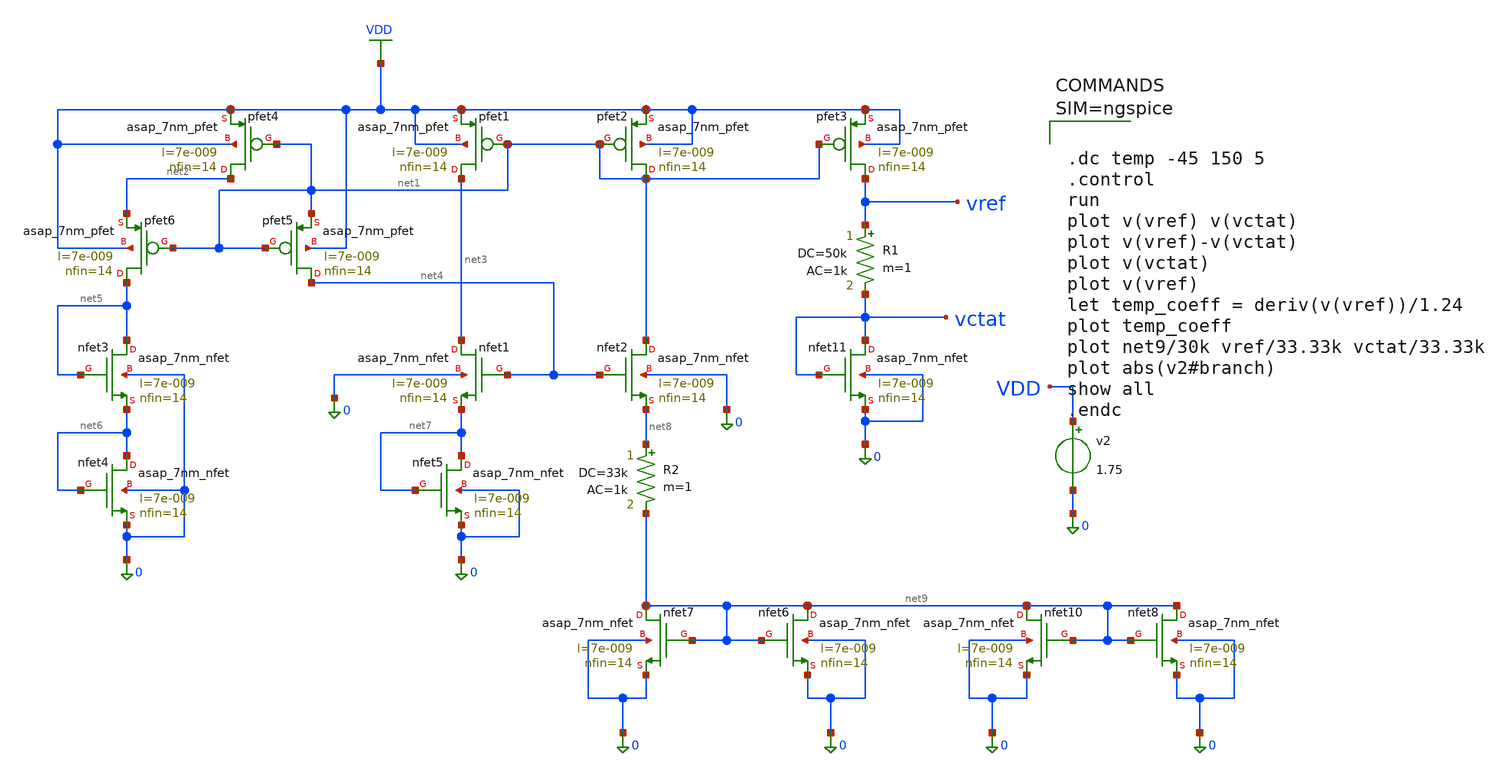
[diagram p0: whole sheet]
** sch_path: 3_Bandgap_Reference/bgrcircuit.sch
**.subckt bgrcircuit
Xpfet1 net3 net1 VDD VDD asap_7nm_pfet l=7e-009 nfin=14
Xnfet1 net3 net4 net7 0 asap_7nm_nfet l=7e-009 nfin=14
Xpfet2 net1 net1 VDD VDD asap_7nm_pfet l=7e-009 nfin=14
Xpfet3 vref net1 VDD VDD asap_7nm_pfet l=7e-009 nfin=14
Xpfet4 net2 net1 VDD VDD asap_7nm_pfet l=7e-009 nfin=14
Xpfet5 net4 net1 net1 VDD asap_7nm_pfet l=7e-009 nfin=14
Xpfet6 net5 net1 net2 VDD asap_7nm_pfet l=7e-009 nfin=14
Xnfet2 net1 net4 net8 0 asap_7nm_nfet l=7e-009 nfin=14
Xnfet3 net5 net5 net6 0 asap_7nm_nfet l=7e-009 nfin=14
Xnfet4 net6 net6 0 0 asap_7nm_nfet l=7e-009 nfin=14
Xnfet5 net7 net7 0 0 asap_7nm_nfet l=7e-009 nfin=14
R2 net8 net9 33k ac=1k m=1
R1 vref vctat 50k ac=1k m=1
Xnfet6 net9 net9 0 0 asap_7nm_nfet l=7e-009 nfin=14
Xnfet7 net9 net9 0 0 asap_7nm_nfet l=7e-009 nfin=14
Xnfet8 net9 net9 0 0 asap_7nm_nfet l=7e-009 nfin=14
Xnfet10 net9 net9 0 0 asap_7nm_nfet l=7e-009 nfin=14
Xnfet11 vctat vctat 0 0 asap_7nm_nfet l=7e-009 nfin=14
v2 VDD 0 1.75
**** begin user architecture code



.dc temp -45 150 5
.control
run
plot v(vref) v(vctat)
plot v(vref)-v(vctat)
plot v(vctat)
plot v(vref)
let temp_coeff = deriv(v(vref))/1.24
plot temp_coeff
plot net9/30k vref/33.33k vctat/33.33k
plot abs(v2#branch)
show all
.endc



**** end user architecture code
**.ends
.GLOBAL VDD
.end
